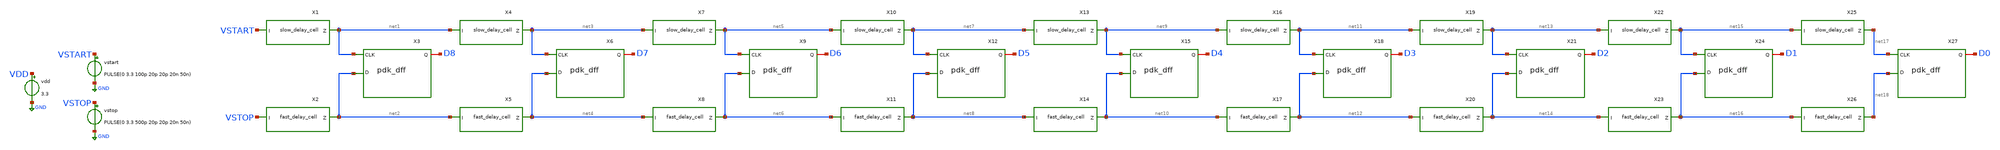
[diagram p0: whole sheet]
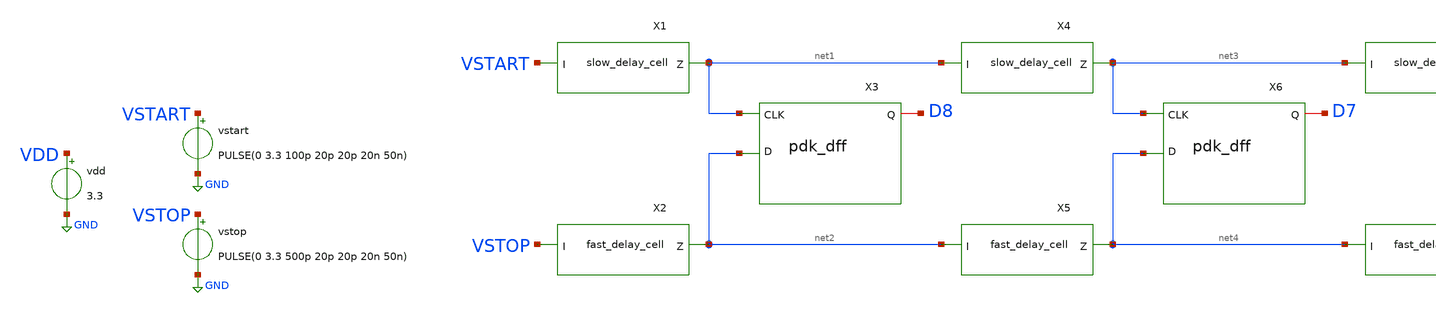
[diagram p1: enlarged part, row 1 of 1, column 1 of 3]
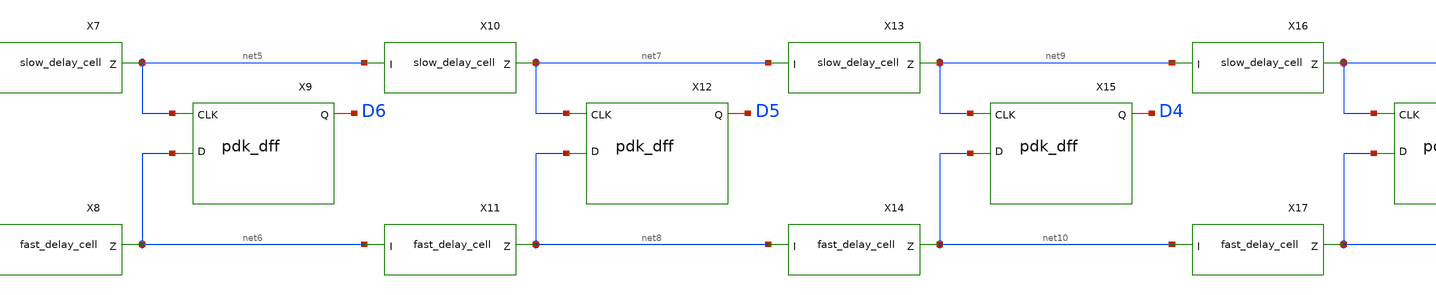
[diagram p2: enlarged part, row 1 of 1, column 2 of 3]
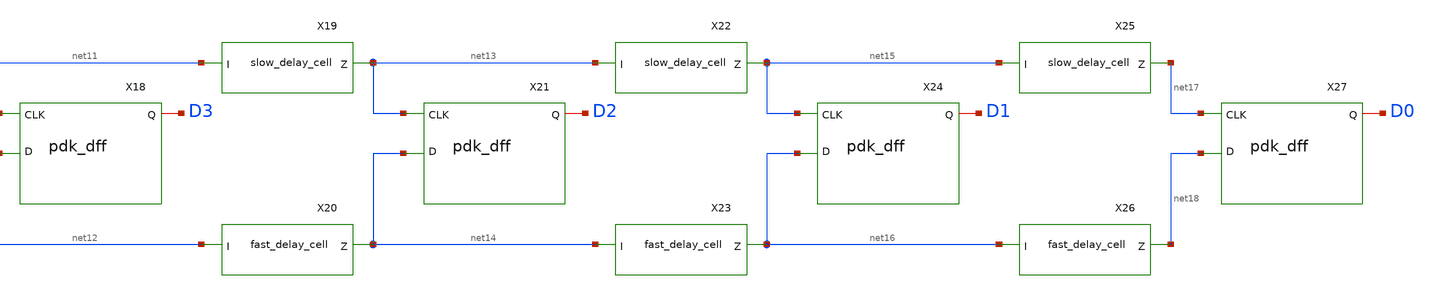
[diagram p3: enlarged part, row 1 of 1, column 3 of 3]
** sch_path: schem/fine_delay_line_test.sch
**.subckt fine_delay_line_test
X1 VSTART net1 VDD VDD 0 0 gf180mcu_fd_sc_mcu7t5v0__dlya_4
X2 VSTOP net2 VDD VDD 0 0 gf180mcu_fd_sc_mcu7t5v0__dlya_1
X3 net2 net1 D8 VDD VDD 0 0 gf180mcu_fd_sc_mcu7t5v0__dffq_1
X4 net1 net3 VDD VDD 0 0 gf180mcu_fd_sc_mcu7t5v0__dlya_4
X5 net2 net4 VDD VDD 0 0 gf180mcu_fd_sc_mcu7t5v0__dlya_1
X6 net4 net3 D7 VDD VDD 0 0 gf180mcu_fd_sc_mcu7t5v0__dffq_1
X7 net3 net5 VDD VDD 0 0 gf180mcu_fd_sc_mcu7t5v0__dlya_4
X8 net4 net6 VDD VDD 0 0 gf180mcu_fd_sc_mcu7t5v0__dlya_1
X9 net6 net5 D6 VDD VDD 0 0 gf180mcu_fd_sc_mcu7t5v0__dffq_1
X10 net5 net7 VDD VDD 0 0 gf180mcu_fd_sc_mcu7t5v0__dlya_4
X11 net6 net8 VDD VDD 0 0 gf180mcu_fd_sc_mcu7t5v0__dlya_1
X12 net8 net7 D5 VDD VDD 0 0 gf180mcu_fd_sc_mcu7t5v0__dffq_1
X13 net7 net9 VDD VDD 0 0 gf180mcu_fd_sc_mcu7t5v0__dlya_4
X14 net8 net10 VDD VDD 0 0 gf180mcu_fd_sc_mcu7t5v0__dlya_1
X15 net10 net9 D4 VDD VDD 0 0 gf180mcu_fd_sc_mcu7t5v0__dffq_1
X16 net9 net11 VDD VDD 0 0 gf180mcu_fd_sc_mcu7t5v0__dlya_4
X17 net10 net12 VDD VDD 0 0 gf180mcu_fd_sc_mcu7t5v0__dlya_1
X18 net12 net11 D3 VDD VDD 0 0 gf180mcu_fd_sc_mcu7t5v0__dffq_1
X19 net11 net13 VDD VDD 0 0 gf180mcu_fd_sc_mcu7t5v0__dlya_4
X20 net12 net14 VDD VDD 0 0 gf180mcu_fd_sc_mcu7t5v0__dlya_1
X21 net14 net13 D2 VDD VDD 0 0 gf180mcu_fd_sc_mcu7t5v0__dffq_1
X22 net13 net15 VDD VDD 0 0 gf180mcu_fd_sc_mcu7t5v0__dlya_4
X23 net14 net16 VDD VDD 0 0 gf180mcu_fd_sc_mcu7t5v0__dlya_1
X24 net16 net15 D1 VDD VDD 0 0 gf180mcu_fd_sc_mcu7t5v0__dffq_1
X25 net15 net17 VDD VDD 0 0 gf180mcu_fd_sc_mcu7t5v0__dlya_4
X26 net16 net18 VDD VDD 0 0 gf180mcu_fd_sc_mcu7t5v0__dlya_1
X27 net18 net17 D0 VDD VDD 0 0 gf180mcu_fd_sc_mcu7t5v0__dffq_1
vstart VSTART GND PULSE(0 3.3 100p 20p 20p 20n 50n)
vstop VSTOP GND PULSE(0 3.3 500p 20p 20p 20n 50n)
vdd VDD GND 3.3
**** begin user architecture code


.temp 25
.tran 1p 15n 0 1p

.meas tran b8 FIND v(d8) AT=12n
.meas tran b7 FIND v(d7) AT=12n
.meas tran b6 FIND v(d6) AT=12n
.meas tran b5 FIND v(d5) AT=12n
.meas tran b4 FIND v(d4) AT=12n
.meas tran b3 FIND v(d3) AT=12n
.meas tran b2 FIND v(d2) AT=12n
.meas tran b1 FIND v(d1) AT=12n
.meas tran b0 FIND v(d0) AT=12n





.include /usr/local/share/pdk/gf180mcuD/libs.tech/ngspice/design.ngspice
.lib /usr/local/share/pdk/gf180mcuD/libs.tech/ngspice/sm141064.ngspice typical
.include /usr/local/share/pdk/gf180mcuD/libs.ref/gf180mcu_fd_sc_mcu7t5v0/spice/gf180mcu_fd_sc_mcu7t5v0.spice


**** end user architecture code
**.ends
.GLOBAL GND
.end
